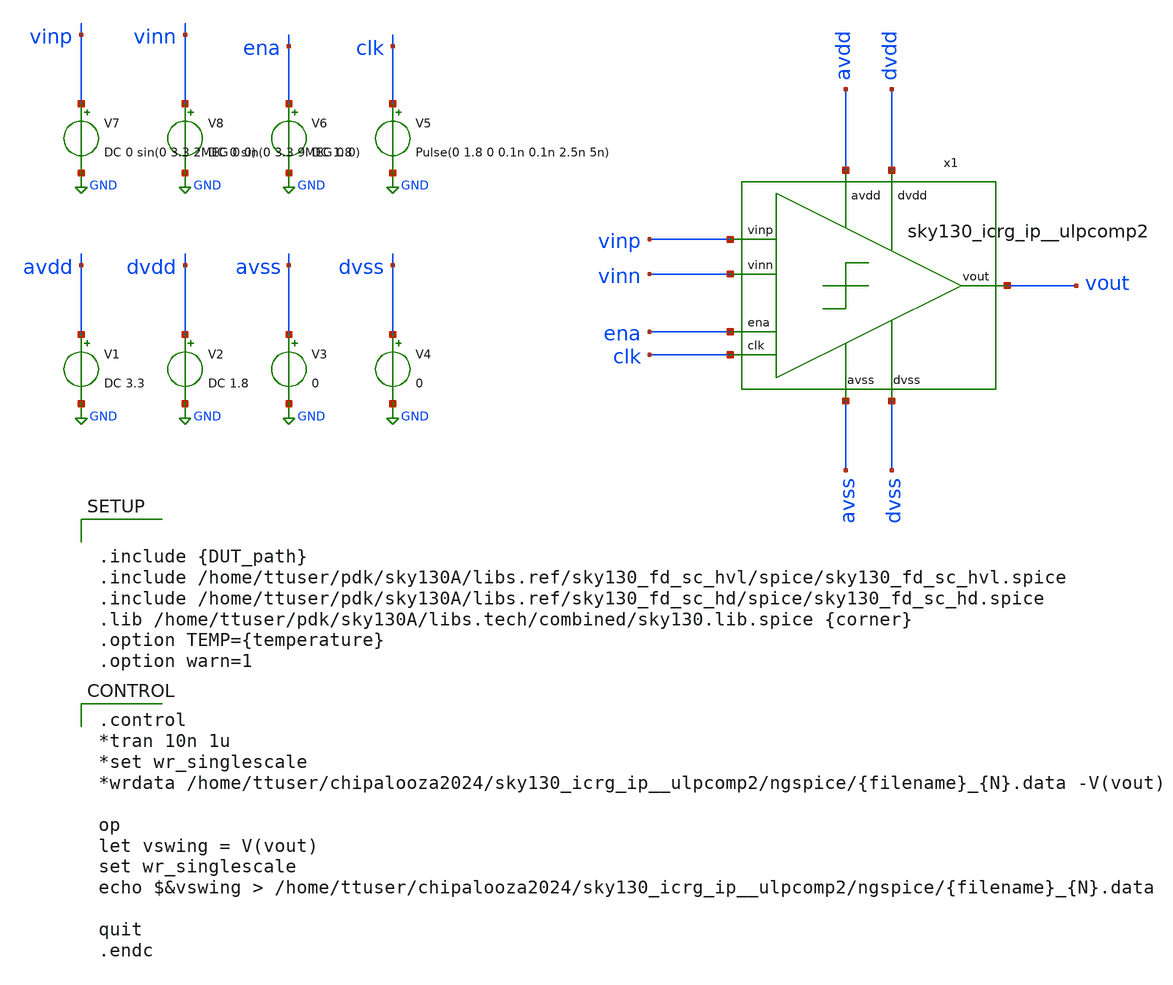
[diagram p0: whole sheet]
** sch_path: cace/vol_swing.sch
**.subckt vol_swing
x1 dvdd avdd ena vout vinn vinp clk dvss avss sky130_icrg_ip__ulpcomp2
V1 avdd GND DC 3.3
V2 dvdd GND DC 1.8
V3 avss GND 0
V4 dvss GND 0
V5 clk GND Pulse(0 1.8 0 0.1n 0.1n 2.5n 5n)
V6 ena GND DC 1.8
V7 vinp GND DC 0 sin(0 3.3 2MEG 0 0)
V8 vinn GND DC 0 sin(0 3.3 9MEG 0 0)
**** begin user architecture code


.include {DUT_path}
.include /home/ttuser/pdk/sky130A/libs.ref/sky130_fd_sc_hvl/spice/sky130_fd_sc_hvl.spice
.include /home/ttuser/pdk/sky130A/libs.ref/sky130_fd_sc_hd/spice/sky130_fd_sc_hd.spice
.lib /home/ttuser/pdk/sky130A/libs.tech/combined/sky130.lib.spice {corner}
.option TEMP={temperature}
.option warn=1


.control
*tran 10n 1u
*set wr_singlescale
*wrdata /home/ttuser/chipalooza2024/sky130_icrg_ip__ulpcomp2/ngspice/{filename}_{N}.data -V(vout)

op
let vswing = V(vout)
set wr_singlescale
echo $&vswing > /home/ttuser/chipalooza2024/sky130_icrg_ip__ulpcomp2/ngspice/{filename}_{N}.data

quit
.endc

**** end user architecture code
**.ends
.GLOBAL GND
.end
